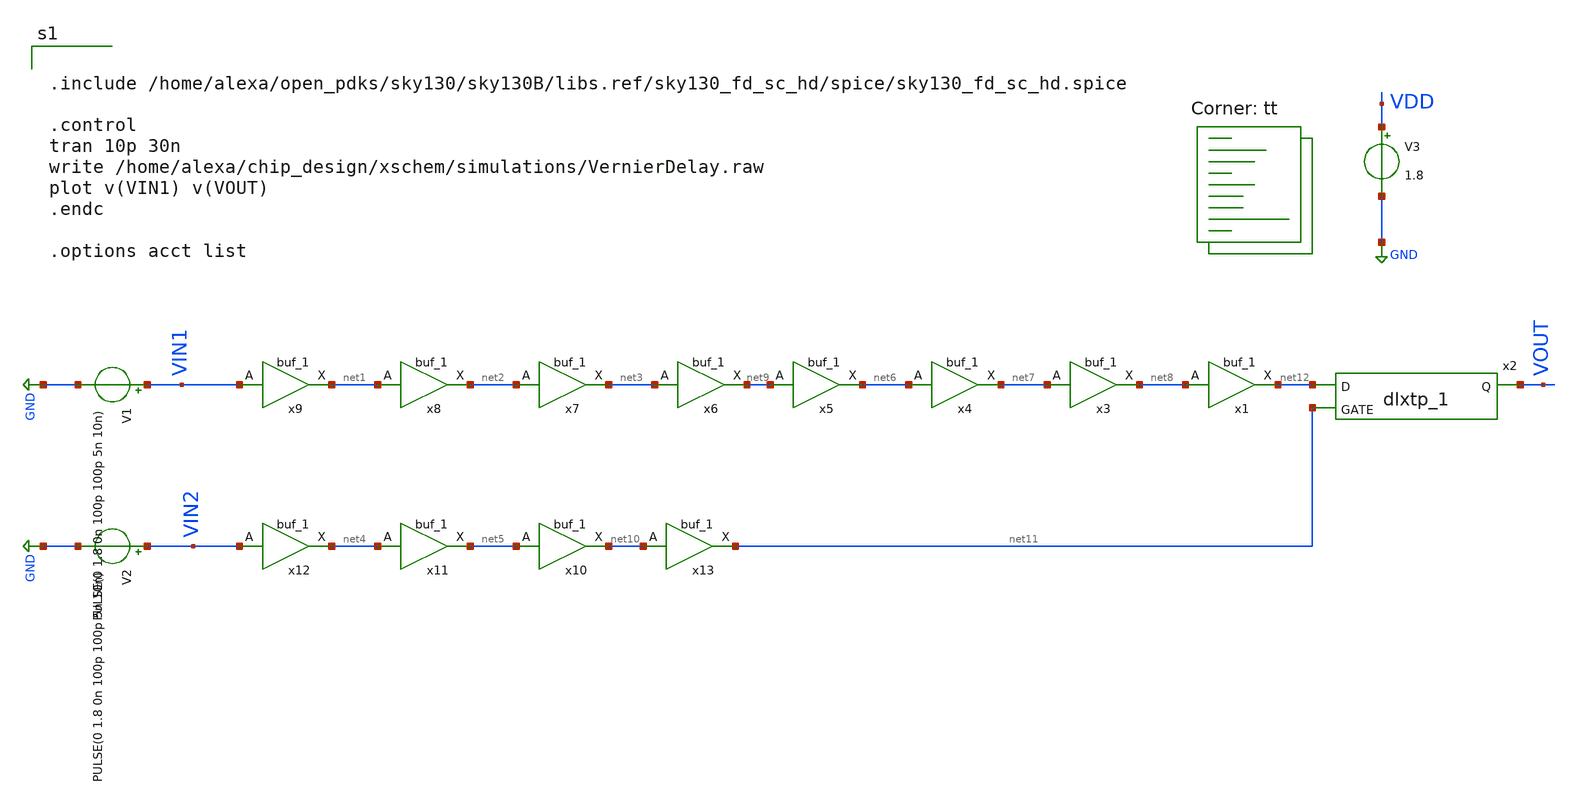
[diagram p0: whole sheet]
** sch_path: xschem/projects/SingleVernier.sch
* Copyright 2021 Stefan Frederik Schippers
* Licensed under the Apache License, Version 2.0 (the "License");
* you may not use this file except in compliance with the License.
* You may obtain a copy of the License at
* https://www.apache.org/licenses/LICENSE-2.0
* Unless required by applicable law or agreed to in writing, software
* distributed under the License is distributed on an "AS IS" BASIS,
* WITHOUT WARRANTIES OR CONDITIONS OF ANY KIND, either express or implied.
* See the License for the specific language governing permissions and
* limitations under the License.
**.subckt SingleVernier
V1 VIN1 GND PULSE(0 1.8 0n 100p 100p 5n 10n)
V2 VIN2 GND PULSE(0 1.8 0n 100p 100p 5n 10n)
V3 VDD GND 1.8
x2 net12 net11 0 0 VDD VDD VOUT sky130_fd_sc_hd__dlxtp_1
x10 net5 GND GND VDD VDD net10 sky130_fd_sc_hd__buf_1
x11 net4 GND GND VDD VDD net5 sky130_fd_sc_hd__buf_1
x12 VIN2 GND GND VDD VDD net4 sky130_fd_sc_hd__buf_1
x6 net3 GND GND VDD VDD net9 sky130_fd_sc_hd__buf_1
x7 net2 GND GND VDD VDD net3 sky130_fd_sc_hd__buf_1
x8 net1 GND GND VDD VDD net2 sky130_fd_sc_hd__buf_1
x9 VIN1 GND GND VDD VDD net1 sky130_fd_sc_hd__buf_1
x1 net8 GND GND VDD VDD net12 sky130_fd_sc_hd__buf_1
x3 net7 GND GND VDD VDD net8 sky130_fd_sc_hd__buf_1
x4 net6 GND GND VDD VDD net7 sky130_fd_sc_hd__buf_1
x5 net9 GND GND VDD VDD net6 sky130_fd_sc_hd__buf_1
x13 net10 GND GND VDD VDD net11 sky130_fd_sc_hd__buf_1
**** begin user architecture code


.include /home/alexa/open_pdks/sky130/sky130B/libs.ref/sky130_fd_sc_hd/spice/sky130_fd_sc_hd.spice

.control
tran 10p 30n
write /home/alexa/chip_design/xschem/simulations/VernierDelay.raw
plot v(VIN1) v(VOUT)
.endc

.options acct list


.lib $::SKYWATER_MODELS/sky130.lib.spice tt
**** end user architecture code
**.ends
.GLOBAL GND
.end
